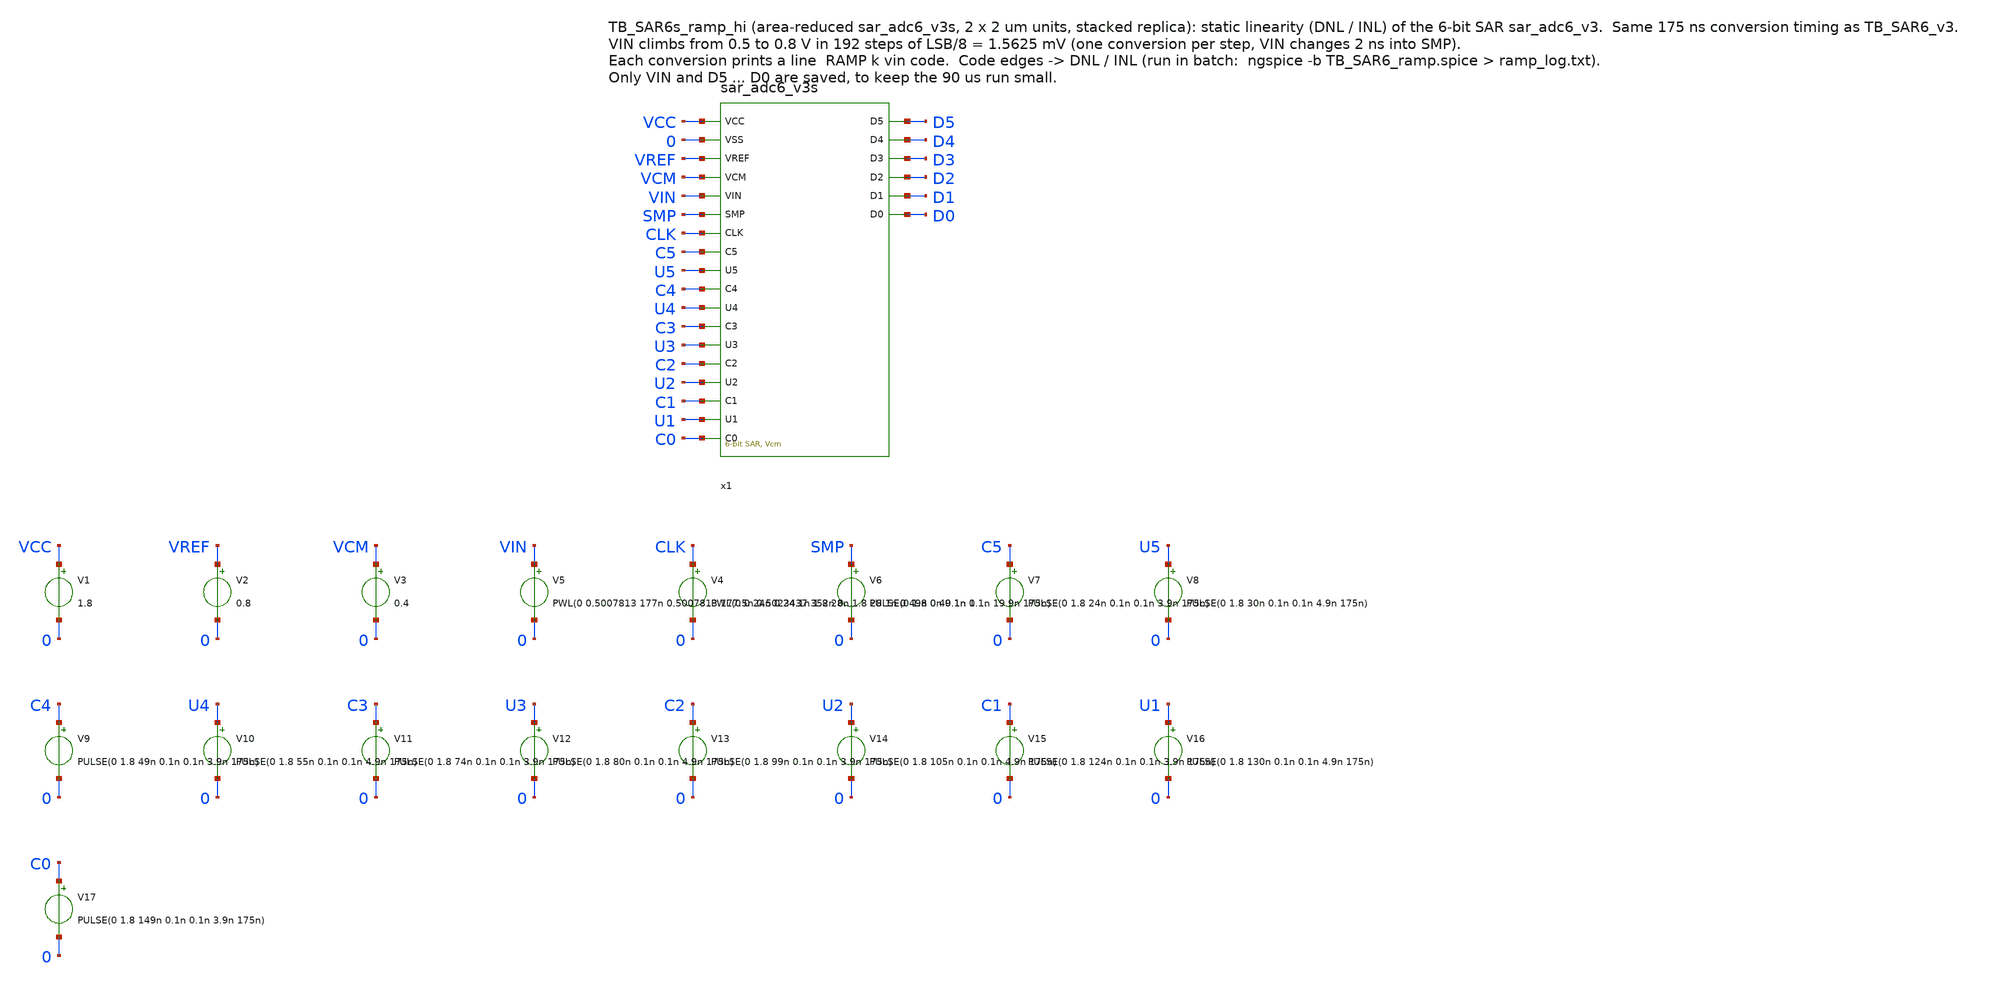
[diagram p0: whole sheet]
** sch_path: SAR_improved/TB_SAR6s_ramp_hi.sch
**.subckt TB_SAR6s_ramp_hi
x1 VCC 0 VREF VCM VIN SMP CLK C5 U5 C4 U4 C3 U3 C2 U2 C1 U1 C0 D5 D4 D3 D2 D1 D0 sar_adc6_v3s
V1 VCC 0 1.8
V2 VREF 0 0.8
V3 VCM 0 0.4
V5 VIN 0 PWL(0 0.5007813 177n 0.5007813 177.5n 0.5023437 352n 0.5023437 352.5n 0.5039062 527n
+ 0.5039062 527.5n 0.5054688 702n 0.5054688 702.5n 0.5070313 877n 0.5070313 877.5n 0.5085938 1052n 0.5085938
+ 1052.5n 0.5101562 1227n 0.5101562 1227.5n 0.5117188 1402n 0.5117188 1402.5n 0.5132813 1577n 0.5132813
+ 1577.5n 0.5148438 1752n 0.5148438 1752.5n 0.5164063 1927n 0.5164063 1927.5n 0.5179687 2102n 0.5179687
+ 2102.5n 0.5195312 2277n 0.5195312 2277.5n 0.5210938 2452n 0.5210938 2452.5n 0.5226563 2627n 0.5226563
+ 2627.5n 0.5242188 2802n 0.5242188 2802.5n 0.5257812 2977n 0.5257812 2977.5n 0.5273438 3152n 0.5273438
+ 3152.5n 0.5289063 3327n 0.5289063 3327.5n 0.5304688 3502n 0.5304688 3502.5n 0.5320313 3677n 0.5320313
+ 3677.5n 0.5335937 3852n 0.5335937 3852.5n 0.5351562 4027n 0.5351562 4027.5n 0.5367188 4202n 0.5367188
+ 4202.5n 0.5382813 4377n 0.5382813 4377.5n 0.5398438 4552n 0.5398438 4552.5n 0.5414062 4727n 0.5414062
+ 4727.5n 0.5429688 4902n 0.5429688 4902.5n 0.5445313 5077n 0.5445313 5077.5n 0.5460938 5252n 0.5460938
+ 5252.5n 0.5476563 5427n 0.5476563 5427.5n 0.5492187 5602n 0.5492187 5602.5n 0.5507812 5777n 0.5507812
+ 5777.5n 0.5523438 5952n 0.5523438 5952.5n 0.5539063 6127n 0.5539063 6127.5n 0.5554688 6302n 0.5554688
+ 6302.5n 0.5570312 6477n 0.5570312 6477.5n 0.5585938 6652n 0.5585938 6652.5n 0.5601563 6827n 0.5601563
+ 6827.5n 0.5617188 7002n 0.5617188 7002.5n 0.5632813 7177n 0.5632813 7177.5n 0.5648437 7352n 0.5648437
+ 7352.5n 0.5664062 7527n 0.5664062 7527.5n 0.5679688 7702n 0.5679688 7702.5n 0.5695313 7877n 0.5695313
+ 7877.5n 0.5710938 8052n 0.5710938 8052.5n 0.5726562 8227n 0.5726562 8227.5n 0.5742188 8402n 0.5742188
+ 8402.5n 0.5757813 8577n 0.5757813 8577.5n 0.5773438 8752n 0.5773438 8752.5n 0.5789063 8927n 0.5789063
+ 8927.5n 0.5804687 9102n 0.5804687 9102.5n 0.5820312 9277n 0.5820312 9277.5n 0.5835938 9452n 0.5835938
+ 9452.5n 0.5851563 9627n 0.5851563 9627.5n 0.5867188 9802n 0.5867188 9802.5n 0.5882812 9977n 0.5882812
+ 9977.5n 0.5898438 10152n 0.5898438 10152.5n 0.5914063 10327n 0.5914063 10327.5n 0.5929688 10502n 0.5929688
+ 10502.5n 0.5945313 10677n 0.5945313 10677.5n 0.5960937 10852n 0.5960937 10852.5n 0.5976562 11027n 0.5976562
+ 11027.5n 0.5992188 11202n 0.5992188 11202.5n 0.6007813 11377n 0.6007813 11377.5n 0.6023438 11552n 0.6023438
+ 11552.5n 0.6039063 11727n 0.6039063 11727.5n 0.6054688 11902n 0.6054688 11902.5n 0.6070313 12077n 0.6070313
+ 12077.5n 0.6085938 12252n 0.6085938 12252.5n 0.6101563 12427n 0.6101563 12427.5n 0.6117188 12602n 0.6117188
+ 12602.5n 0.6132812 12777n 0.6132812 12777.5n 0.6148438 12952n 0.6148438 12952.5n 0.6164063 13127n 0.6164063
+ 13127.5n 0.6179688 13302n 0.6179688 13302.5n 0.6195313 13477n 0.6195313 13477.5n 0.6210938 13652n 0.6210938
+ 13652.5n 0.6226563 13827n 0.6226563 13827.5n 0.6242188 14002n 0.6242188 14002.5n 0.6257813 14177n 0.6257813
+ 14177.5n 0.6273438 14352n 0.6273438 14352.5n 0.6289062 14527n 0.6289062 14527.5n 0.6304688 14702n 0.6304688
+ 14702.5n 0.6320313 14877n 0.6320313 14877.5n 0.6335938 15052n 0.6335938 15052.5n 0.6351563 15227n 0.6351563
+ 15227.5n 0.6367188 15402n 0.6367188 15402.5n 0.6382813 15577n 0.6382813 15577.5n 0.6398438 15752n 0.6398438
+ 15752.5n 0.6414063 15927n 0.6414063 15927.5n 0.6429688 16102n 0.6429688 16102.5n 0.6445312 16277n 0.6445312
+ 16277.5n 0.6460938 16452n 0.6460938 16452.5n 0.6476563 16627n 0.6476563 16627.5n 0.6492188 16802n 0.6492188
+ 16802.5n 0.6507813 16977n 0.6507813 16977.5n 0.6523438 17152n 0.6523438 17152.5n 0.6539063 17327n 0.6539063
+ 17327.5n 0.6554688 17502n 0.6554688 17502.5n 0.6570313 17677n 0.6570313 17677.5n 0.6585938 17852n 0.6585938
+ 17852.5n 0.6601562 18027n 0.6601562 18027.5n 0.6617188 18202n 0.6617188 18202.5n 0.6632813 18377n 0.6632813
+ 18377.5n 0.6648438 18552n 0.6648438 18552.5n 0.6664063 18727n 0.6664063 18727.5n 0.6679688 18902n 0.6679688
+ 18902.5n 0.6695313 19077n 0.6695313 19077.5n 0.6710938 19252n 0.6710938 19252.5n 0.6726563 19427n 0.6726563
+ 19427.5n 0.6742188 19602n 0.6742188 19602.5n 0.6757812 19777n 0.6757812 19777.5n 0.6773438 19952n 0.6773438
+ 19952.5n 0.6789063 20127n 0.6789063 20127.5n 0.6804688 20302n 0.6804688 20302.5n 0.6820313 20477n 0.6820313
+ 20477.5n 0.6835938 20652n 0.6835938 20652.5n 0.6851563 20827n 0.6851563 20827.5n 0.6867188 21002n 0.6867188
+ 21002.5n 0.6882813 21177n 0.6882813 21177.5n 0.6898438 21352n 0.6898438 21352.5n 0.6914062 21527n 0.6914062
+ 21527.5n 0.6929688 21702n 0.6929688 21702.5n 0.6945313 21877n 0.6945313 21877.5n 0.6960938 22052n 0.6960938
+ 22052.5n 0.6976563 22227n 0.6976563 22227.5n 0.6992188 22402n 0.6992188 22402.5n 0.7007813 22577n 0.7007813
+ 22577.5n 0.7023438 22752n 0.7023438 22752.5n 0.7039063 22927n 0.7039063 22927.5n 0.7054688 23102n 0.7054688
+ 23102.5n 0.7070312 23277n 0.7070312 23277.5n 0.7085938 23452n 0.7085938 23452.5n 0.7101563 23627n 0.7101563
+ 23627.5n 0.7117188 23802n 0.7117188 23802.5n 0.7132813 23977n 0.7132813 23977.5n 0.7148438 24152n 0.7148438
+ 24152.5n 0.7164063 24327n 0.7164063 24327.5n 0.7179688 24502n 0.7179688 24502.5n 0.7195313 24677n 0.7195313
+ 24677.5n 0.7210938 24852n 0.7210938 24852.5n 0.7226562 25027n 0.7226562 25027.5n 0.7242188 25202n 0.7242188
+ 25202.5n 0.7257813 25377n 0.7257813 25377.5n 0.7273438 25552n 0.7273438 25552.5n 0.7289063 25727n 0.7289063
+ 25727.5n 0.7304688 25902n 0.7304688 25902.5n 0.7320313 26077n 0.7320313 26077.5n 0.7335938 26252n 0.7335938
+ 26252.5n 0.7351563 26427n 0.7351563 26427.5n 0.7367188 26602n 0.7367188 26602.5n 0.7382812 26777n 0.7382812
+ 26777.5n 0.7398438 26952n 0.7398438 26952.5n 0.7414063 27127n 0.7414063 27127.5n 0.7429688 27302n 0.7429688
+ 27302.5n 0.7445313 27477n 0.7445313 27477.5n 0.7460938 27652n 0.7460938 27652.5n 0.7476563 27827n 0.7476563
+ 27827.5n 0.7492188 28002n 0.7492188 28002.5n 0.7507813 28177n 0.7507813 28177.5n 0.7523438 28352n 0.7523438
+ 28352.5n 0.7539062 28527n 0.7539062 28527.5n 0.7554688 28702n 0.7554688 28702.5n 0.7570313 28877n 0.7570313
+ 28877.5n 0.7585938 29052n 0.7585938 29052.5n 0.7601563 29227n 0.7601563 29227.5n 0.7617188 29402n 0.7617188
+ 29402.5n 0.7632813 29577n 0.7632813 29577.5n 0.7648438 29752n 0.7648438 29752.5n 0.7664063 29927n 0.7664063
+ 29927.5n 0.7679688 30102n 0.7679688 30102.5n 0.7695312 30277n 0.7695312 30277.5n 0.7710938 30452n 0.7710938
+ 30452.5n 0.7726563 30627n 0.7726563 30627.5n 0.7742188 30802n 0.7742188 30802.5n 0.7757813 30977n 0.7757813
+ 30977.5n 0.7773438 31152n 0.7773438 31152.5n 0.7789063 31327n 0.7789063 31327.5n 0.7804688 31502n 0.7804688
+ 31502.5n 0.7820313 31677n 0.7820313 31677.5n 0.7835938 31852n 0.7835938 31852.5n 0.7851562 32027n 0.7851562
+ 32027.5n 0.7867188 32202n 0.7867188 32202.5n 0.7882813 32377n 0.7882813 32377.5n 0.7898438 32552n 0.7898438
+ 32552.5n 0.7914063 32727n 0.7914063 32727.5n 0.7929688 32902n 0.7929688 32902.5n 0.7945313 33077n 0.7945313
+ 33077.5n 0.7960938 33252n 0.7960938 33252.5n 0.7976563 33427n 0.7976563 33427.5n 0.7992188)
V4 CLK 0 PWL(0 0 24n 0 24.1n 1.8 28n 1.8 28.1n 0 49n 0 49.1n 1.8 53n 1.8 53.1n 0 74n 0 74.1n 1.8 78n
+ 1.8 78.1n 0 99n 0 99.1n 1.8 103n 1.8 103.1n 0 124n 0 124.1n 1.8 128n 1.8 128.1n 0 149n 0 149.1n 1.8
+ 153n 1.8 153.1n 0 175n 0) r=0
V6 SMP 0 PULSE(0 1.8 0n 0.1n 0.1n 19.9n 175n)
V7 C5 0 PULSE(0 1.8 24n 0.1n 0.1n 3.9n 175n)
V8 U5 0 PULSE(0 1.8 30n 0.1n 0.1n 4.9n 175n)
V9 C4 0 PULSE(0 1.8 49n 0.1n 0.1n 3.9n 175n)
V10 U4 0 PULSE(0 1.8 55n 0.1n 0.1n 4.9n 175n)
V11 C3 0 PULSE(0 1.8 74n 0.1n 0.1n 3.9n 175n)
V12 U3 0 PULSE(0 1.8 80n 0.1n 0.1n 4.9n 175n)
V13 C2 0 PULSE(0 1.8 99n 0.1n 0.1n 3.9n 175n)
V14 U2 0 PULSE(0 1.8 105n 0.1n 0.1n 4.9n 175n)
V15 C1 0 PULSE(0 1.8 124n 0.1n 0.1n 3.9n 175n)
V16 U1 0 PULSE(0 1.8 130n 0.1n 0.1n 4.9n 175n)
V17 C0 0 PULSE(0 1.8 149n 0.1n 0.1n 3.9n 175n)
**** begin user architecture code

.lib /home/ttuser/pdk/sky130A/libs.tech/combined/sky130.lib.spice tt
.option method=gear reltol=1e-4
.control
save v(VIN) v(D5) v(D4) v(D3) v(D2) v(D1) v(D0)
tran 0.1n 33600n
let code = 0*v(D0)
let code = code + 32*ceil((v(D5)-0.9)/10)
let code = code + 16*ceil((v(D4)-0.9)/10)
let code = code + 8*ceil((v(D3)-0.9)/10)
let code = code + 4*ceil((v(D2)-0.9)/10)
let code = code + 2*ceil((v(D1)-0.9)/10)
let code = code + 1*ceil((v(D0)-0.9)/10)
let k = 0
while k < 192
  let tr = k*175e-9 + 165e-9
  meas tran ck find code at=$&tr
  meas tran vk find v(VIN) at=$&tr
  echo RAMP $&k $&vk $&ck
  let k = k + 1
end
plot code
.endc

**** end user architecture code
**.ends
.end
